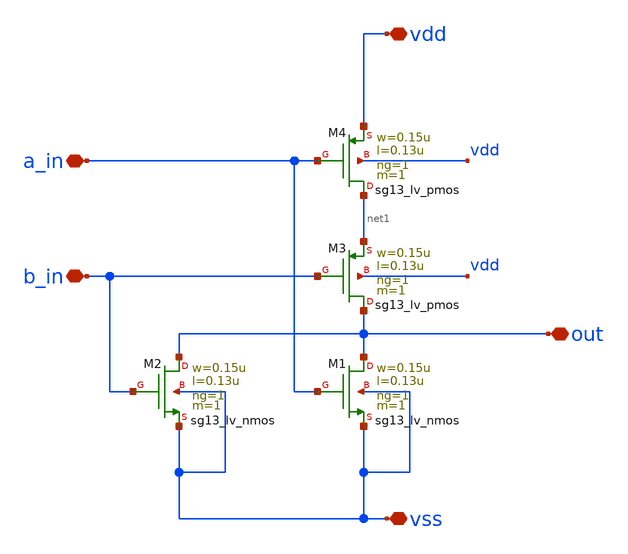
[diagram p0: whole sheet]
** sch_path: design/blocks/norgate/schematic/norgate.sch
**.subckt norgate vdd vss a_in b_in out
*.iopin vdd
*.iopin vss
*.iopin a_in
*.iopin b_in
*.iopin out
XM1 out a_in vss vss sg13_lv_nmos w=0.15u l=0.13u ng=1 m=1 mm_ok=1
XM2 out b_in vss vss sg13_lv_nmos w=0.15u l=0.13u ng=1 m=1 mm_ok=1
XM3 out b_in net1 vdd sg13_lv_pmos w=0.15u l=0.13u ng=1 m=1 mm_ok=1
XM4 net1 a_in vdd vdd sg13_lv_pmos w=0.15u l=0.13u ng=1 m=1 mm_ok=1
**.ends
.end
